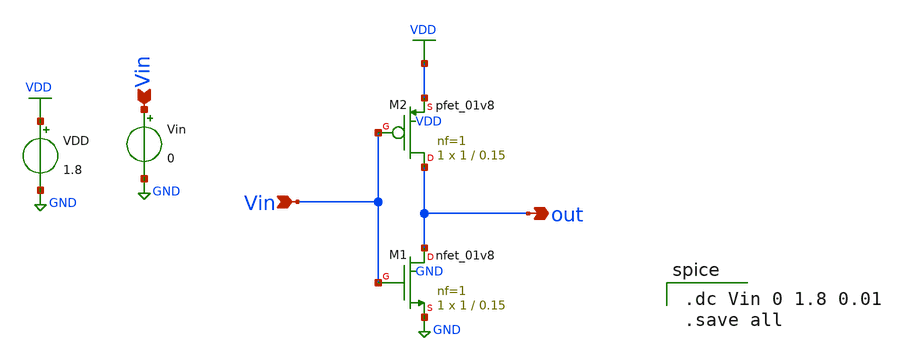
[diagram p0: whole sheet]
** sch_path: xschem/inverter_tutorialv1.sch
**.subckt inverter_tutorialv1 Vin out Vin
*.ipin Vin
*.opin out
*.ipin Vin
XM1 out Vin GND GND sky130_fd_pr__nfet_01v8 L=0.15 W=1 nf=1 ad='int((nf+1)/2) * W/nf * 0.29' as='int((nf+2)/2) * W/nf * 0.29'
+ pd='2*int((nf+1)/2) * (W/nf + 0.29)' ps='2*int((nf+2)/2) * (W/nf + 0.29)' nrd='0.29 / W' nrs='0.29 / W'
+ sa=0 sb=0 sd=0 mult=1 m=1
XM2 out Vin VDD VDD sky130_fd_pr__pfet_01v8 L=0.15 W=1 nf=1 ad='int((nf+1)/2) * W/nf * 0.29' as='int((nf+2)/2) * W/nf * 0.29'
+ pd='2*int((nf+1)/2) * (W/nf + 0.29)' ps='2*int((nf+2)/2) * (W/nf + 0.29)' nrd='0.29 / W' nrs='0.29 / W'
+ sa=0 sb=0 sd=0 mult=1 m=1
VDD VDD GND 1.8
Vin Vin GND 0
**** begin user architecture code

** opencircuitdesign pdks install
.lib $::SKYWATER_MODELS/sky130.lib.spice tt



.dc Vin 0 1.8 0.01
.save all


**** end user architecture code
**.ends
.GLOBAL GND
.GLOBAL VDD
.end
